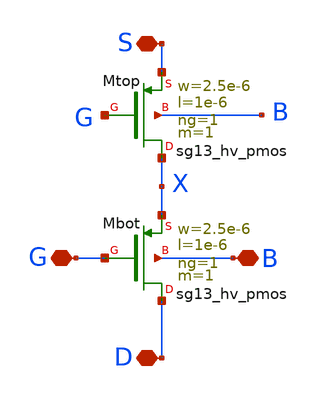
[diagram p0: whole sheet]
** sch_path: macros/comparator/schematic/xschem/p1_2.sch
**.subckt p1_2 G D S B
*.iopin G
*.iopin D
*.iopin S
*.iopin B
XMbot D G X B sg13_hv_pmos w=2.5e-6 l=1e-6 ng=1 m=1 mm_ok=1
XMtop X G S B sg13_hv_pmos w=2.5e-6 l=1e-6 ng=1 m=1 mm_ok=1
**.ends
.end
